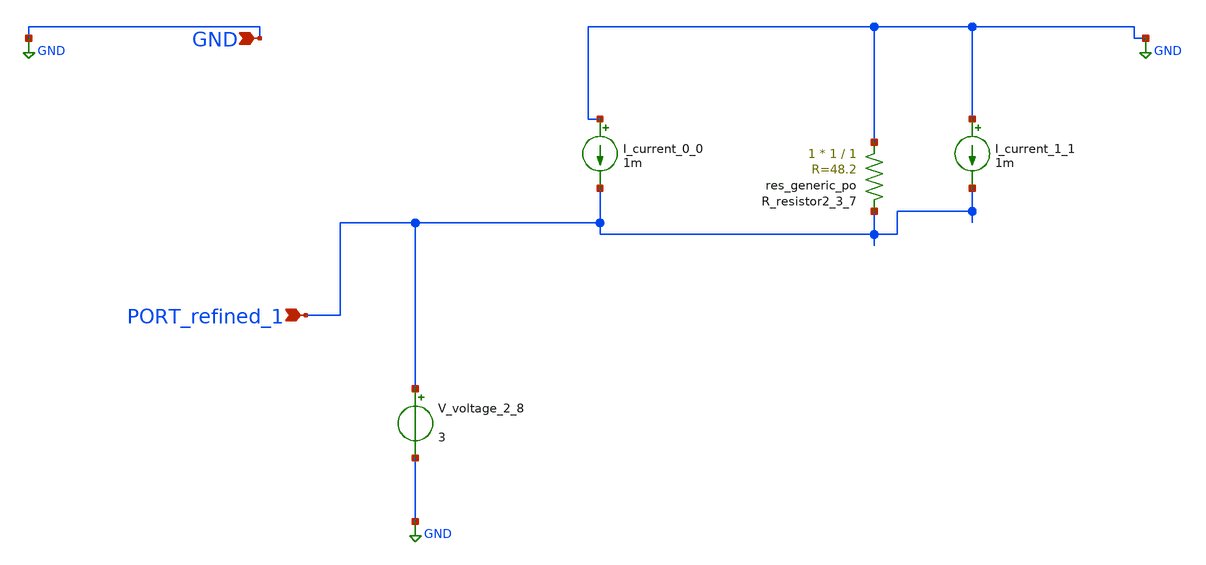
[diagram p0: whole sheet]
** sch_path: schematics/AMSNet/74.sch
**.subckt 74 PORT_refined_1 GND
*.ipin PORT_refined_1
*.ipin GND
I_current_0_0 GND PORT_refined_1 1m
I_current_1_1 GND PORT_refined_1 1m
XR_resistor2_3_7 GND PORT_refined_1 sky130_fd_pr__res_generic_po W=1 L=1 m=1
V_voltage_2_8 PORT_refined_1 GND 3
**.ends
.GLOBAL GND
.end
